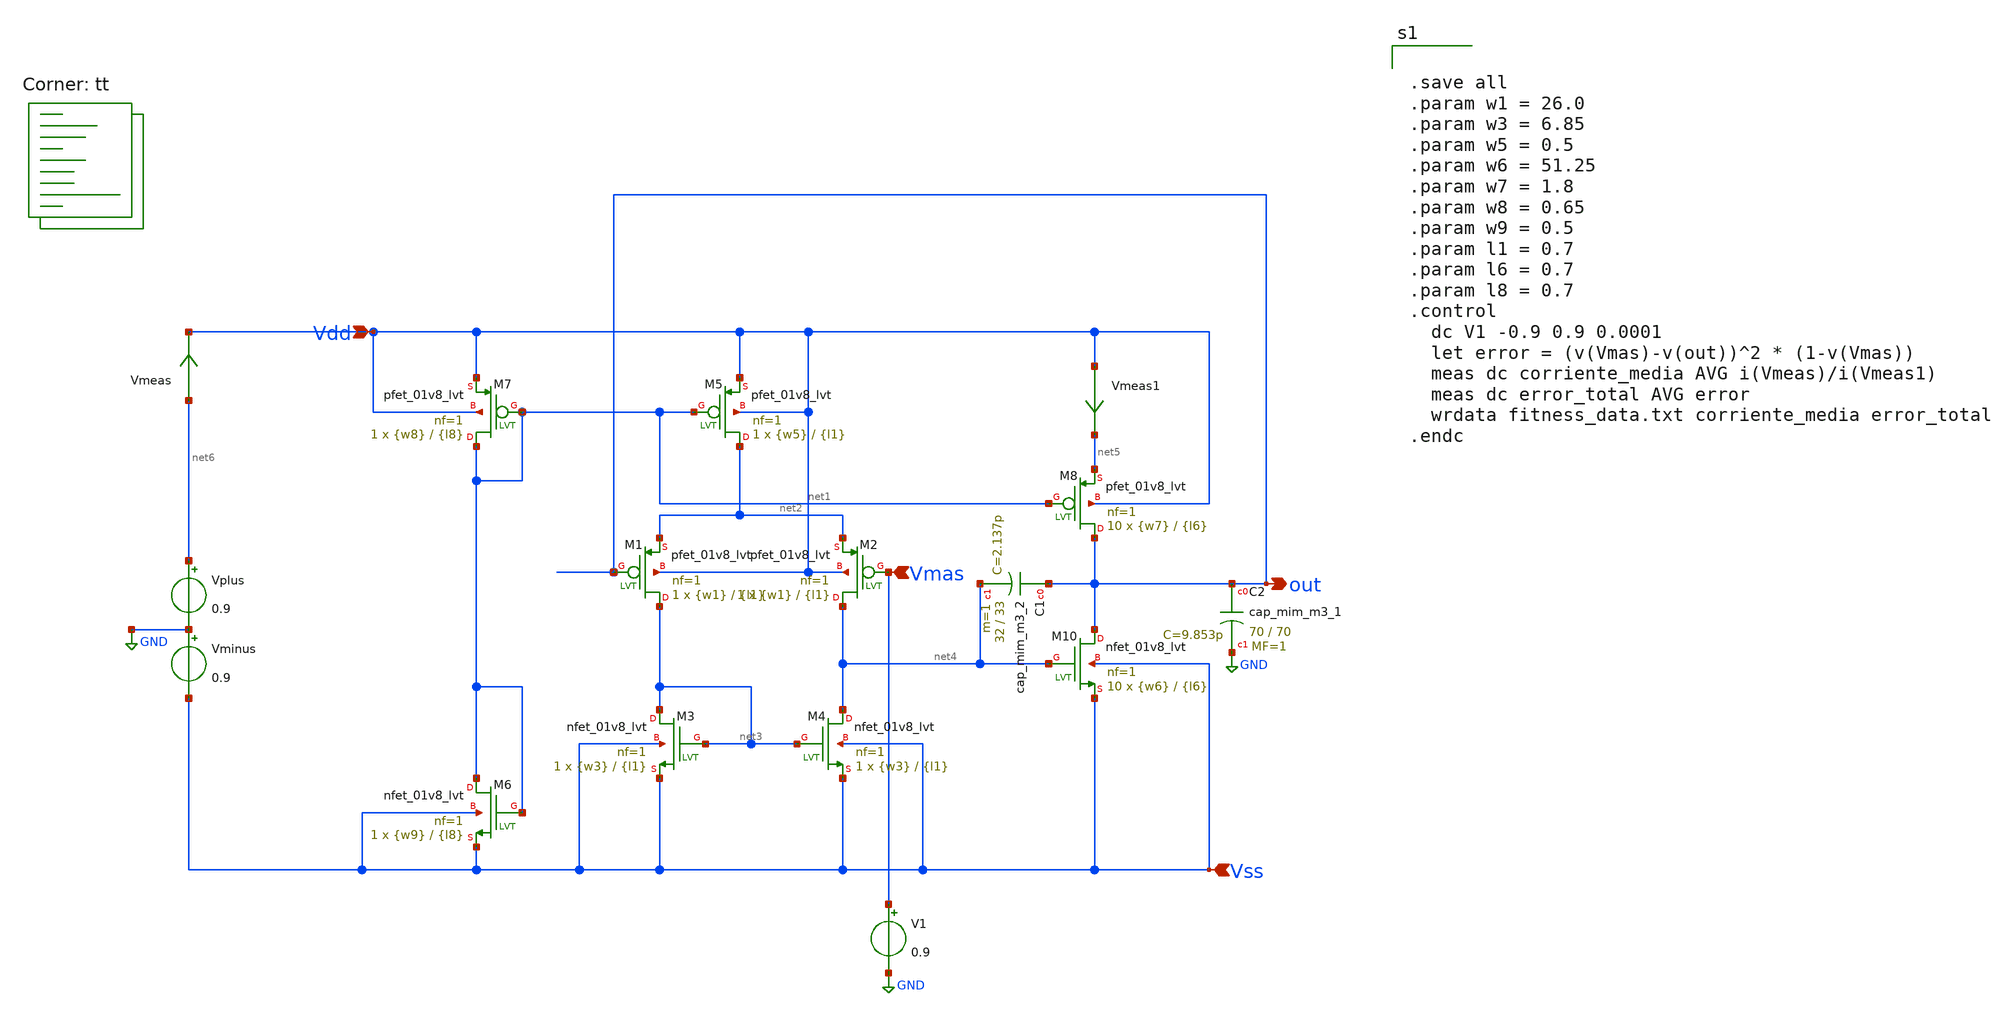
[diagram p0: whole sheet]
** sch_path: examples/SH/op_sim.sch
**.subckt op_sim Vdd Vmas Vss out
*.ipin Vdd
*.ipin Vmas
*.ipin Vss
*.opin out
XM10 out net4 Vss Vss sky130_fd_pr__nfet_01v8_lvt L={l6} W={w6} nf=1 ad='int((1 + 1)/2) * {w6} / 1 * 0.29'
+ as='int((1 + 2)/2) * {w6} / 1 * 0.29' pd='2*int((1 + 1)/2) * ({w6} / 1 + 0.29)' ps='2*int((1 + 2)/2) * ({w6} / 1 + 0.29)'
+ nrd='0.29 / {w6} ' nrs='0.29 / {w6} ' sa=0 sb=0 sd=0 mult=10 m=10
XM8 out net1 net5 Vdd sky130_fd_pr__pfet_01v8_lvt L={l6} W={w7} nf=1 ad='int((1 + 1)/2) * {w7} / 1 * 0.29'
+ as='int((1 + 2)/2) * {w7} / 1 * 0.29' pd='2*int((1 + 1)/2) * ({w7} / 1 + 0.29)' ps='2*int((1 + 2)/2) * ({w7} / 1 + 0.29)'
+ nrd='0.29 / {w7} ' nrs='0.29 / {w7} ' sa=0 sb=0 sd=0 mult=10 m=10
XM7 net1 net1 Vdd Vdd sky130_fd_pr__pfet_01v8_lvt L={l8} W={w8} nf=1 ad='int((1 + 1)/2) * {w8} / 1 * 0.29'
+ as='int((1 + 2)/2) * {w8} / 1 * 0.29' pd='2*int((1 + 1)/2) * ({w8} / 1 + 0.29)' ps='2*int((1 + 2)/2) * ({w8} / 1 + 0.29)'
+ nrd='0.29 / {w8} ' nrs='0.29 / {w8} ' sa=0 sb=0 sd=0 mult=1 m=1
XM3 net3 net3 Vss Vss sky130_fd_pr__nfet_01v8_lvt L={l1} W={w3} nf=1 ad='int((1 + 1)/2) * {w3} / 1 * 0.29'
+ as='int((1 + 2)/2) * {w3} / 1 * 0.29' pd='2*int((1 + 1)/2) * ({w3} / 1 + 0.29)' ps='2*int((1 + 2)/2) * ({w3} / 1 + 0.29)'
+ nrd='0.29 / {w3} ' nrs='0.29 / {w3} ' sa=0 sb=0 sd=0 mult=1 m=1
XM4 net4 net3 Vss Vss sky130_fd_pr__nfet_01v8_lvt L={l1} W={w3} nf=1 ad='int((1 + 1)/2) * {w3} / 1 * 0.29'
+ as='int((1 + 2)/2) * {w3} / 1 * 0.29' pd='2*int((1 + 1)/2) * ({w3} / 1 + 0.29)' ps='2*int((1 + 2)/2) * ({w3} / 1 + 0.29)'
+ nrd='0.29 / {w3} ' nrs='0.29 / {w3} ' sa=0 sb=0 sd=0 mult=1 m=1
XM5 net2 net1 Vdd Vdd sky130_fd_pr__pfet_01v8_lvt L={l1} W={w5} nf=1 ad='int((1 + 1)/2) * {w5} / 1 * 0.29'
+ as='int((1 + 2)/2) * {w5} / 1 * 0.29' pd='2*int((1 + 1)/2) * ({w5} / 1 + 0.29)' ps='2*int((1 + 2)/2) * ({w5} / 1 + 0.29)'
+ nrd='0.29 / {w5} ' nrs='0.29 / {w5} ' sa=0 sb=0 sd=0 mult=1 m=1
XM1 net3 out net2 Vdd sky130_fd_pr__pfet_01v8_lvt L={l1} W={w1} nf=1 ad='int((1 + 1)/2) * {w1} / 1 * 0.29'
+ as='int((1 + 2)/2) * {w1} / 1 * 0.29' pd='2*int((1 + 1)/2) * ({w1} / 1 + 0.29)' ps='2*int((1 + 2)/2) * ({w1} / 1 + 0.29)'
+ nrd='0.29 / {w1} ' nrs='0.29 / {w1} ' sa=0 sb=0 sd=0 mult=1 m=1
XM2 net4 Vmas net2 Vdd sky130_fd_pr__pfet_01v8_lvt L={l1} W={w1} nf=1 ad='int((1 + 1)/2) * {w1} / 1 * 0.29'
+ as='int((1 + 2)/2) * {w1} / 1 * 0.29' pd='2*int((1 + 1)/2) * ({w1} / 1 + 0.29)' ps='2*int((1 + 2)/2) * ({w1} / 1 + 0.29)'
+ nrd='0.29 / {w1} ' nrs='0.29 / {w1} ' sa=0 sb=0 sd=0 mult=1 m=1
XC1 out net4 sky130_fd_pr__cap_mim_m3_2 W=32 L=33 MF=1 m=1
XC2 out GND sky130_fd_pr__cap_mim_m3_1 W=70 L=70 MF=1 m=1
XM6 net1 net1 Vss Vss sky130_fd_pr__nfet_01v8_lvt L={l8} W={w9} nf=1 ad='int((1 + 1)/2) * {w9} / 1 * 0.29'
+ as='int((1 + 2)/2) * {w9} / 1 * 0.29' pd='2*int((1 + 1)/2) * ({w9} / 1 + 0.29)' ps='2*int((1 + 2)/2) * ({w9} / 1 + 0.29)'
+ nrd='0.29 / {w9} ' nrs='0.29 / {w9} ' sa=0 sb=0 sd=0 mult=1 m=1
Vplus net6 GND 0.9
Vminus GND Vss 0.9
Vmeas net6 Vdd 0
.save i(vmeas)
V1 Vmas GND 0.9
Vmeas1 Vdd net5 0
.save i(vmeas1)
**** begin user architecture code
.lib $::SKYWATER_MODELS/sky130.lib.spice tt


.save all
.param w1 = 26.0
.param w3 = 6.85
.param w5 = 0.5
.param w6 = 51.25
.param w7 = 1.8
.param w8 = 0.65
.param w9 = 0.5
.param l1 = 0.7
.param l6 = 0.7
.param l8 = 0.7
.control
  dc V1 -0.9 0.9 0.0001
  let error = (v(Vmas)-v(out))^2 * (1-v(Vmas))
  meas dc corriente_media AVG i(Vmeas)/i(Vmeas1)
  meas dc error_total AVG error
  wrdata fitness_data.txt corriente_media error_total
.endc


**** end user architecture code
**.ends
.GLOBAL GND
.end
